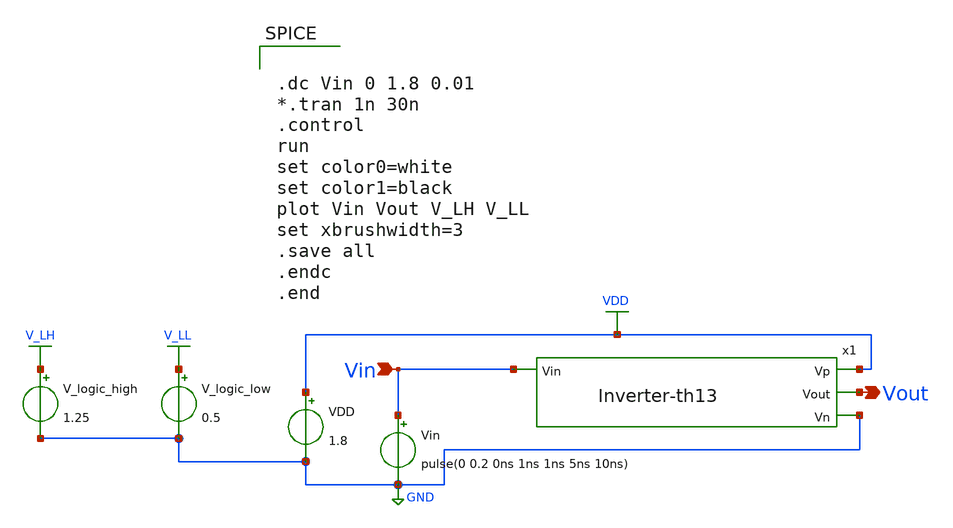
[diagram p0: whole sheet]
** sch_path: xschem/Vth_sch/Pre_layout/Inverter-th12.sch
**.subckt Inverter-th12 Vin Vout
*.ipin Vin
*.opin Vout
VDD VDD GND 1.8
Vin Vin GND pulse(0 0.2 0ns 1ns 1ns 5ns 10ns)
V_logic_high V_LH GND 1.25
V_logic_low V_LL GND 0.5
x1 VDD Vin Vout GND Inverter-th13
**** begin user architecture code


.lib /usr/local/share/pdk/sky130A/libs.tech/ngspice/sky130.lib.spice tt

.save all





.dc Vin 0 1.8 0.01
*.tran 1n 30n
.control
run
set color0=white
set color1=black
plot Vin Vout V_LH V_LL
set xbrushwidth=3
.save all
.endc
.end


**** end user architecture code
**.ends

* expanding   symbol:  /home/exotic/Desktop/ASIC_ADC/xschem/Vth_sch/Symbol/Inverter-th13.sym # of
*+ pins=4
** sym_path: xschem/Vth_sch/Symbol/Inverter-th13.sym
** sch_path: xschem/Vth_sch/Symbol/Inverter-th13.sch
.subckt Inverter-th13 Vp Vin Vout Vn
*.ipin Vin
*.opin Vout
*.opin Vp
*.opin Vn
XM1 Vout Vin Vp Vp sky130_fd_pr__pfet_01v8 L=0.15 W=6.98 nf=1 ad='int((nf+1)/2) * W/nf * 0.29' as='int((nf+2)/2) * W/nf * 0.29'
+ pd='2*int((nf+1)/2) * (W/nf + 0.29)' ps='2*int((nf+2)/2) * (W/nf + 0.29)' nrd='0.29 / W' nrs='0.29 / W'
+ sa=0 sb=0 sd=0 mult=1 m=1
XM2 Vout Vin net1 net1 sky130_fd_pr__nfet_01v8 L=22 W=0.36 nf=1 ad='int((nf+1)/2) * W/nf * 0.29' as='int((nf+2)/2) * W/nf * 0.29'
+ pd='2*int((nf+1)/2) * (W/nf + 0.29)' ps='2*int((nf+2)/2) * (W/nf + 0.29)' nrd='0.29 / W' nrs='0.29 / W'
+ sa=0 sb=0 sd=0 mult=1 m=1
XM3 Vn Vn net1 net1 sky130_fd_pr__pfet_01v8 L=0.15 W=6.98 nf=1 ad='int((nf+1)/2) * W/nf * 0.29' as='int((nf+2)/2) * W/nf * 0.29'
+ pd='2*int((nf+1)/2) * (W/nf + 0.29)' ps='2*int((nf+2)/2) * (W/nf + 0.29)' nrd='0.29 / W' nrs='0.29 / W'
+ sa=0 sb=0 sd=0 mult=1 m=1
.ends

.GLOBAL VDD
.GLOBAL GND
.GLOBAL V_LH
.GLOBAL V_LL
.end
